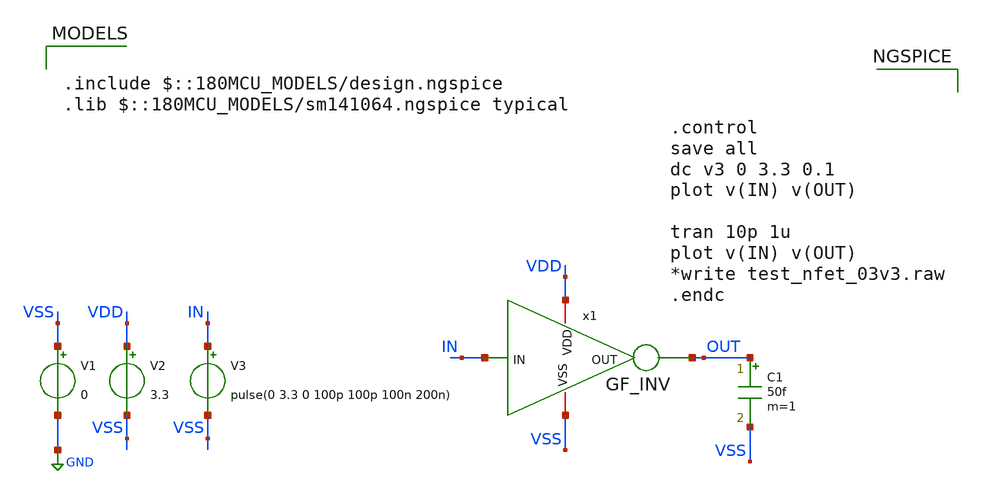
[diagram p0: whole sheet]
** sch_path: Clock_Generator_PAKISTAN_02/Schematics/GF_INV_TB.sch
**.subckt GF_INV_TB
x1 VSS VDD OUT IN GF_INV
C1 OUT VSS 50f m=1
V1 VSS GND 0
V2 VDD VSS 3.3
V3 IN VSS pulse(0 3.3 0 100p 100p 100n 200n)
**** begin user architecture code

.include $::180MCU_MODELS/design.ngspice
.lib $::180MCU_MODELS/sm141064.ngspice typical




.control
save all
dc v3 0 3.3 0.1
plot v(IN) v(OUT)

tran 10p 1u
plot v(IN) v(OUT)
*write test_nfet_03v3.raw
.endc


**** end user architecture code
**.ends

* expanding   symbol:  GF_INV.sym # of pins=4
** sym_path: GF_INV.sym
** sch_path: GF_INV.sch
.subckt GF_INV VSS VDD OUT IN
*.iopin VDD
*.iopin VSS
*.ipin IN
*.opin OUT
XM1 OUT IN VSS VSS nfet_03v3 L=0.56u W=0.56u nf=1 ad='int((nf+1)/2) * W/nf * 0.18u' as='int((nf+2)/2) * W/nf * 0.18u'
+ pd='2*int((nf+1)/2) * (W/nf + 0.18u)' ps='2*int((nf+2)/2) * (W/nf + 0.18u)' nrd='0.18u / W' nrs='0.18u / W'
+ sa=0 sb=0 sd=0 m=1
XM2 OUT IN VDD VDD pfet_03v3 L=0.56u W=1.12u nf=1 ad='int((nf+1)/2) * W/nf * 0.18u' as='int((nf+2)/2) * W/nf * 0.18u'
+ pd='2*int((nf+1)/2) * (W/nf + 0.18u)' ps='2*int((nf+2)/2) * (W/nf + 0.18u)' nrd='0.18u / W' nrs='0.18u / W'
+ sa=0 sb=0 sd=0 m=1
.ends

.GLOBAL GND
.end
